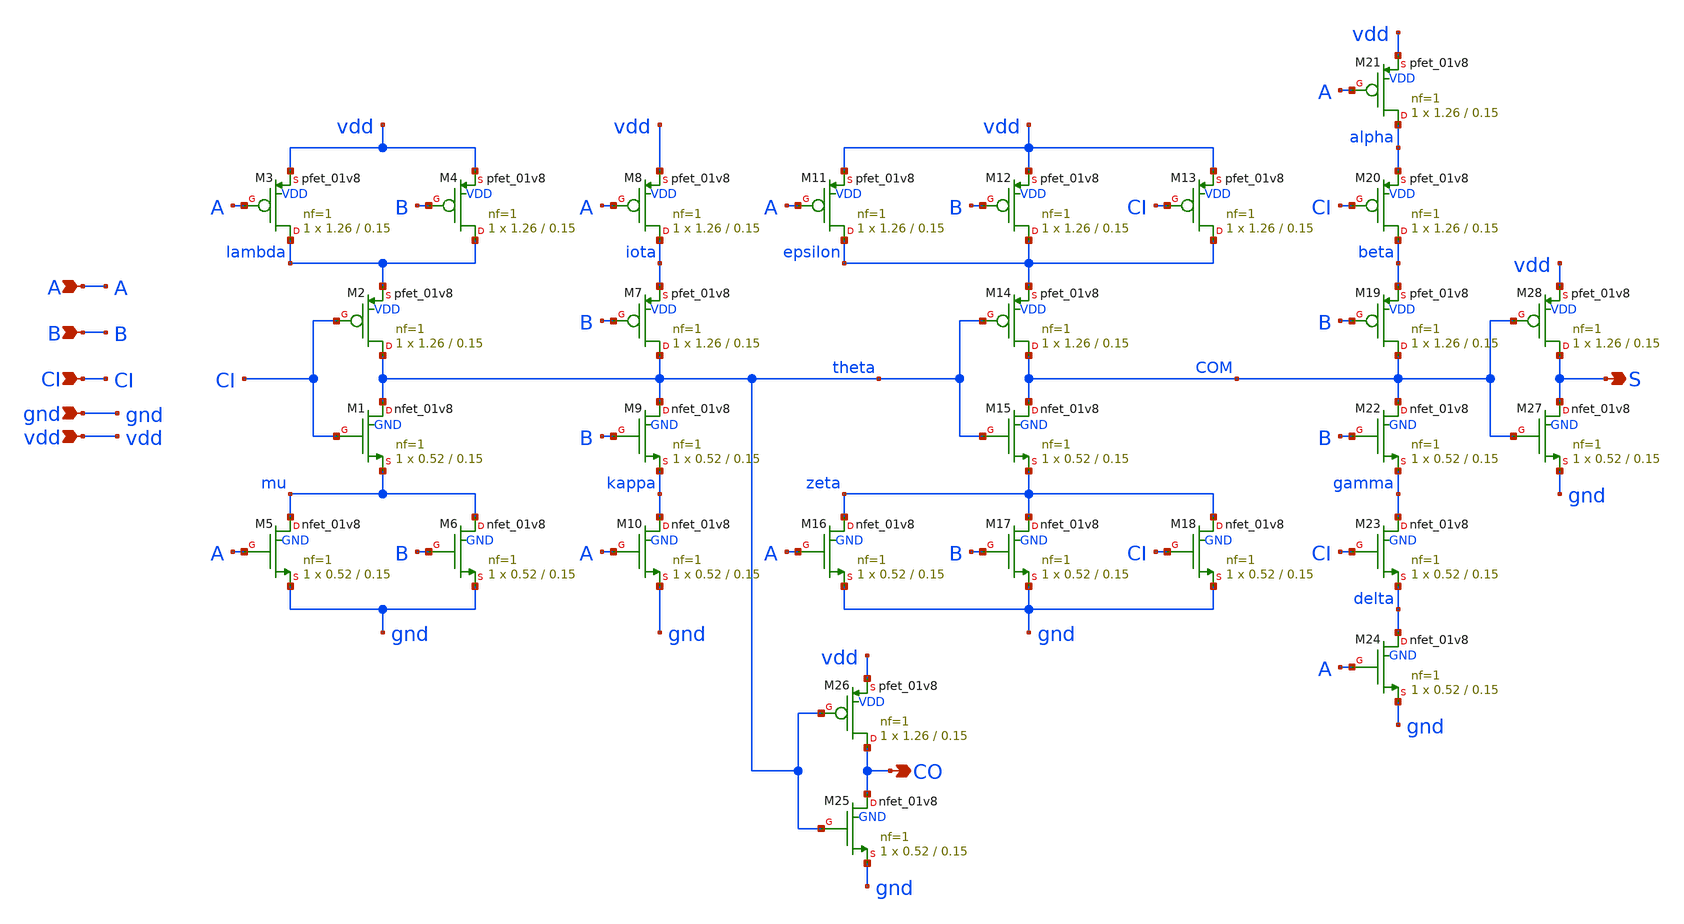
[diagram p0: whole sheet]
** sch_path: xschem/addf.sch
**.subckt addf A B CI S CO vdd gnd
*.ipin A
*.ipin B
*.ipin CI
*.opin S
*.opin CO
*.ipin vdd
*.ipin gnd
XM1 theta CI mu GND sky130_fd_pr__nfet_01v8 L=0.15 W=0.52 nf=1 ad='int((nf+1)/2) * W/nf * 0.29' as='int((nf+2)/2) * W/nf * 0.29'
+ pd='2*int((nf+1)/2) * (W/nf + 0.29)' ps='2*int((nf+2)/2) * (W/nf + 0.29)' nrd='0.29 / W' nrs='0.29 / W'
+ sa=0 sb=0 sd=0 mult=1 m=1
XM2 theta CI lambda VDD sky130_fd_pr__pfet_01v8 L=0.15 W=1.26 nf=1 ad='int((nf+1)/2) * W/nf * 0.29' as='int((nf+2)/2) * W/nf * 0.29'
+ pd='2*int((nf+1)/2) * (W/nf + 0.29)' ps='2*int((nf+2)/2) * (W/nf + 0.29)' nrd='0.29 / W' nrs='0.29 / W'
+ sa=0 sb=0 sd=0 mult=1 m=1
XM3 lambda A vdd VDD sky130_fd_pr__pfet_01v8 L=0.15 W=1.26 nf=1 ad='int((nf+1)/2) * W/nf * 0.29' as='int((nf+2)/2) * W/nf * 0.29'
+ pd='2*int((nf+1)/2) * (W/nf + 0.29)' ps='2*int((nf+2)/2) * (W/nf + 0.29)' nrd='0.29 / W' nrs='0.29 / W'
+ sa=0 sb=0 sd=0 mult=1 m=1
XM4 lambda B vdd VDD sky130_fd_pr__pfet_01v8 L=0.15 W=1.26 nf=1 ad='int((nf+1)/2) * W/nf * 0.29' as='int((nf+2)/2) * W/nf * 0.29'
+ pd='2*int((nf+1)/2) * (W/nf + 0.29)' ps='2*int((nf+2)/2) * (W/nf + 0.29)' nrd='0.29 / W' nrs='0.29 / W'
+ sa=0 sb=0 sd=0 mult=1 m=1
XM5 mu A gnd GND sky130_fd_pr__nfet_01v8 L=0.15 W=0.52 nf=1 ad='int((nf+1)/2) * W/nf * 0.29' as='int((nf+2)/2) * W/nf * 0.29'
+ pd='2*int((nf+1)/2) * (W/nf + 0.29)' ps='2*int((nf+2)/2) * (W/nf + 0.29)' nrd='0.29 / W' nrs='0.29 / W'
+ sa=0 sb=0 sd=0 mult=1 m=1
XM6 mu B gnd GND sky130_fd_pr__nfet_01v8 L=0.15 W=0.52 nf=1 ad='int((nf+1)/2) * W/nf * 0.29' as='int((nf+2)/2) * W/nf * 0.29'
+ pd='2*int((nf+1)/2) * (W/nf + 0.29)' ps='2*int((nf+2)/2) * (W/nf + 0.29)' nrd='0.29 / W' nrs='0.29 / W'
+ sa=0 sb=0 sd=0 mult=1 m=1
XM7 theta B iota VDD sky130_fd_pr__pfet_01v8 L=0.15 W=1.26 nf=1 ad='int((nf+1)/2) * W/nf * 0.29' as='int((nf+2)/2) * W/nf * 0.29'
+ pd='2*int((nf+1)/2) * (W/nf + 0.29)' ps='2*int((nf+2)/2) * (W/nf + 0.29)' nrd='0.29 / W' nrs='0.29 / W'
+ sa=0 sb=0 sd=0 mult=1 m=1
XM8 iota A vdd VDD sky130_fd_pr__pfet_01v8 L=0.15 W=1.26 nf=1 ad='int((nf+1)/2) * W/nf * 0.29' as='int((nf+2)/2) * W/nf * 0.29'
+ pd='2*int((nf+1)/2) * (W/nf + 0.29)' ps='2*int((nf+2)/2) * (W/nf + 0.29)' nrd='0.29 / W' nrs='0.29 / W'
+ sa=0 sb=0 sd=0 mult=1 m=1
XM9 theta B kappa GND sky130_fd_pr__nfet_01v8 L=0.15 W=0.52 nf=1 ad='int((nf+1)/2) * W/nf * 0.29' as='int((nf+2)/2) * W/nf * 0.29'
+ pd='2*int((nf+1)/2) * (W/nf + 0.29)' ps='2*int((nf+2)/2) * (W/nf + 0.29)' nrd='0.29 / W' nrs='0.29 / W'
+ sa=0 sb=0 sd=0 mult=1 m=1
XM10 kappa A gnd GND sky130_fd_pr__nfet_01v8 L=0.15 W=0.52 nf=1 ad='int((nf+1)/2) * W/nf * 0.29' as='int((nf+2)/2) * W/nf * 0.29'
+ pd='2*int((nf+1)/2) * (W/nf + 0.29)' ps='2*int((nf+2)/2) * (W/nf + 0.29)' nrd='0.29 / W' nrs='0.29 / W'
+ sa=0 sb=0 sd=0 mult=1 m=1
XM11 epsilon A vdd VDD sky130_fd_pr__pfet_01v8 L=0.15 W=1.26 nf=1 ad='int((nf+1)/2) * W/nf * 0.29' as='int((nf+2)/2) * W/nf * 0.29'
+ pd='2*int((nf+1)/2) * (W/nf + 0.29)' ps='2*int((nf+2)/2) * (W/nf + 0.29)' nrd='0.29 / W' nrs='0.29 / W'
+ sa=0 sb=0 sd=0 mult=1 m=1
XM12 epsilon B vdd VDD sky130_fd_pr__pfet_01v8 L=0.15 W=1.26 nf=1 ad='int((nf+1)/2) * W/nf * 0.29' as='int((nf+2)/2) * W/nf * 0.29'
+ pd='2*int((nf+1)/2) * (W/nf + 0.29)' ps='2*int((nf+2)/2) * (W/nf + 0.29)' nrd='0.29 / W' nrs='0.29 / W'
+ sa=0 sb=0 sd=0 mult=1 m=1
XM13 epsilon CI vdd VDD sky130_fd_pr__pfet_01v8 L=0.15 W=1.26 nf=1 ad='int((nf+1)/2) * W/nf * 0.29' as='int((nf+2)/2) * W/nf * 0.29'
+ pd='2*int((nf+1)/2) * (W/nf + 0.29)' ps='2*int((nf+2)/2) * (W/nf + 0.29)' nrd='0.29 / W' nrs='0.29 / W'
+ sa=0 sb=0 sd=0 mult=1 m=1
XM14 COM theta epsilon VDD sky130_fd_pr__pfet_01v8 L=0.15 W=1.26 nf=1 ad='int((nf+1)/2) * W/nf * 0.29'
+ as='int((nf+2)/2) * W/nf * 0.29' pd='2*int((nf+1)/2) * (W/nf + 0.29)' ps='2*int((nf+2)/2) * (W/nf + 0.29)'
+ nrd='0.29 / W' nrs='0.29 / W' sa=0 sb=0 sd=0 mult=1 m=1
XM15 COM theta zeta GND sky130_fd_pr__nfet_01v8 L=0.15 W=0.52 nf=1 ad='int((nf+1)/2) * W/nf * 0.29' as='int((nf+2)/2) * W/nf * 0.29'
+ pd='2*int((nf+1)/2) * (W/nf + 0.29)' ps='2*int((nf+2)/2) * (W/nf + 0.29)' nrd='0.29 / W' nrs='0.29 / W'
+ sa=0 sb=0 sd=0 mult=1 m=1
XM16 zeta A gnd GND sky130_fd_pr__nfet_01v8 L=0.15 W=0.52 nf=1 ad='int((nf+1)/2) * W/nf * 0.29' as='int((nf+2)/2) * W/nf * 0.29'
+ pd='2*int((nf+1)/2) * (W/nf + 0.29)' ps='2*int((nf+2)/2) * (W/nf + 0.29)' nrd='0.29 / W' nrs='0.29 / W'
+ sa=0 sb=0 sd=0 mult=1 m=1
XM17 zeta B gnd GND sky130_fd_pr__nfet_01v8 L=0.15 W=0.52 nf=1 ad='int((nf+1)/2) * W/nf * 0.29' as='int((nf+2)/2) * W/nf * 0.29'
+ pd='2*int((nf+1)/2) * (W/nf + 0.29)' ps='2*int((nf+2)/2) * (W/nf + 0.29)' nrd='0.29 / W' nrs='0.29 / W'
+ sa=0 sb=0 sd=0 mult=1 m=1
XM18 zeta CI gnd GND sky130_fd_pr__nfet_01v8 L=0.15 W=0.52 nf=1 ad='int((nf+1)/2) * W/nf * 0.29' as='int((nf+2)/2) * W/nf * 0.29'
+ pd='2*int((nf+1)/2) * (W/nf + 0.29)' ps='2*int((nf+2)/2) * (W/nf + 0.29)' nrd='0.29 / W' nrs='0.29 / W'
+ sa=0 sb=0 sd=0 mult=1 m=1
XM19 COM B beta VDD sky130_fd_pr__pfet_01v8 L=0.15 W=1.26 nf=1 ad='int((nf+1)/2) * W/nf * 0.29' as='int((nf+2)/2) * W/nf * 0.29'
+ pd='2*int((nf+1)/2) * (W/nf + 0.29)' ps='2*int((nf+2)/2) * (W/nf + 0.29)' nrd='0.29 / W' nrs='0.29 / W'
+ sa=0 sb=0 sd=0 mult=1 m=1
XM20 beta CI alpha VDD sky130_fd_pr__pfet_01v8 L=0.15 W=1.26 nf=1 ad='int((nf+1)/2) * W/nf * 0.29' as='int((nf+2)/2) * W/nf * 0.29'
+ pd='2*int((nf+1)/2) * (W/nf + 0.29)' ps='2*int((nf+2)/2) * (W/nf + 0.29)' nrd='0.29 / W' nrs='0.29 / W'
+ sa=0 sb=0 sd=0 mult=1 m=1
XM21 alpha A vdd VDD sky130_fd_pr__pfet_01v8 L=0.15 W=1.26 nf=1 ad='int((nf+1)/2) * W/nf * 0.29' as='int((nf+2)/2) * W/nf * 0.29'
+ pd='2*int((nf+1)/2) * (W/nf + 0.29)' ps='2*int((nf+2)/2) * (W/nf + 0.29)' nrd='0.29 / W' nrs='0.29 / W'
+ sa=0 sb=0 sd=0 mult=1 m=1
XM22 COM B gamma GND sky130_fd_pr__nfet_01v8 L=0.15 W=0.52 nf=1 ad='int((nf+1)/2) * W/nf * 0.29' as='int((nf+2)/2) * W/nf * 0.29'
+ pd='2*int((nf+1)/2) * (W/nf + 0.29)' ps='2*int((nf+2)/2) * (W/nf + 0.29)' nrd='0.29 / W' nrs='0.29 / W'
+ sa=0 sb=0 sd=0 mult=1 m=1
XM23 gamma CI delta GND sky130_fd_pr__nfet_01v8 L=0.15 W=0.52 nf=1 ad='int((nf+1)/2) * W/nf * 0.29' as='int((nf+2)/2) * W/nf * 0.29'
+ pd='2*int((nf+1)/2) * (W/nf + 0.29)' ps='2*int((nf+2)/2) * (W/nf + 0.29)' nrd='0.29 / W' nrs='0.29 / W'
+ sa=0 sb=0 sd=0 mult=1 m=1
XM24 delta A gnd GND sky130_fd_pr__nfet_01v8 L=0.15 W=0.52 nf=1 ad='int((nf+1)/2) * W/nf * 0.29' as='int((nf+2)/2) * W/nf * 0.29'
+ pd='2*int((nf+1)/2) * (W/nf + 0.29)' ps='2*int((nf+2)/2) * (W/nf + 0.29)' nrd='0.29 / W' nrs='0.29 / W'
+ sa=0 sb=0 sd=0 mult=1 m=1
XM25 CO theta gnd GND sky130_fd_pr__nfet_01v8 L=0.15 W=0.52 nf=1 ad='int((nf+1)/2) * W/nf * 0.29' as='int((nf+2)/2) * W/nf * 0.29'
+ pd='2*int((nf+1)/2) * (W/nf + 0.29)' ps='2*int((nf+2)/2) * (W/nf + 0.29)' nrd='0.29 / W' nrs='0.29 / W'
+ sa=0 sb=0 sd=0 mult=1 m=1
XM26 CO theta vdd VDD sky130_fd_pr__pfet_01v8 L=0.15 W=1.26 nf=1 ad='int((nf+1)/2) * W/nf * 0.29' as='int((nf+2)/2) * W/nf * 0.29'
+ pd='2*int((nf+1)/2) * (W/nf + 0.29)' ps='2*int((nf+2)/2) * (W/nf + 0.29)' nrd='0.29 / W' nrs='0.29 / W'
+ sa=0 sb=0 sd=0 mult=1 m=1
XM27 S COM gnd GND sky130_fd_pr__nfet_01v8 L=0.15 W=0.52 nf=1 ad='int((nf+1)/2) * W/nf * 0.29' as='int((nf+2)/2) * W/nf * 0.29'
+ pd='2*int((nf+1)/2) * (W/nf + 0.29)' ps='2*int((nf+2)/2) * (W/nf + 0.29)' nrd='0.29 / W' nrs='0.29 / W'
+ sa=0 sb=0 sd=0 mult=1 m=1
XM28 S COM vdd VDD sky130_fd_pr__pfet_01v8 L=0.15 W=1.26 nf=1 ad='int((nf+1)/2) * W/nf * 0.29' as='int((nf+2)/2) * W/nf * 0.29'
+ pd='2*int((nf+1)/2) * (W/nf + 0.29)' ps='2*int((nf+2)/2) * (W/nf + 0.29)' nrd='0.29 / W' nrs='0.29 / W'
+ sa=0 sb=0 sd=0 mult=1 m=1
**.ends
.end
